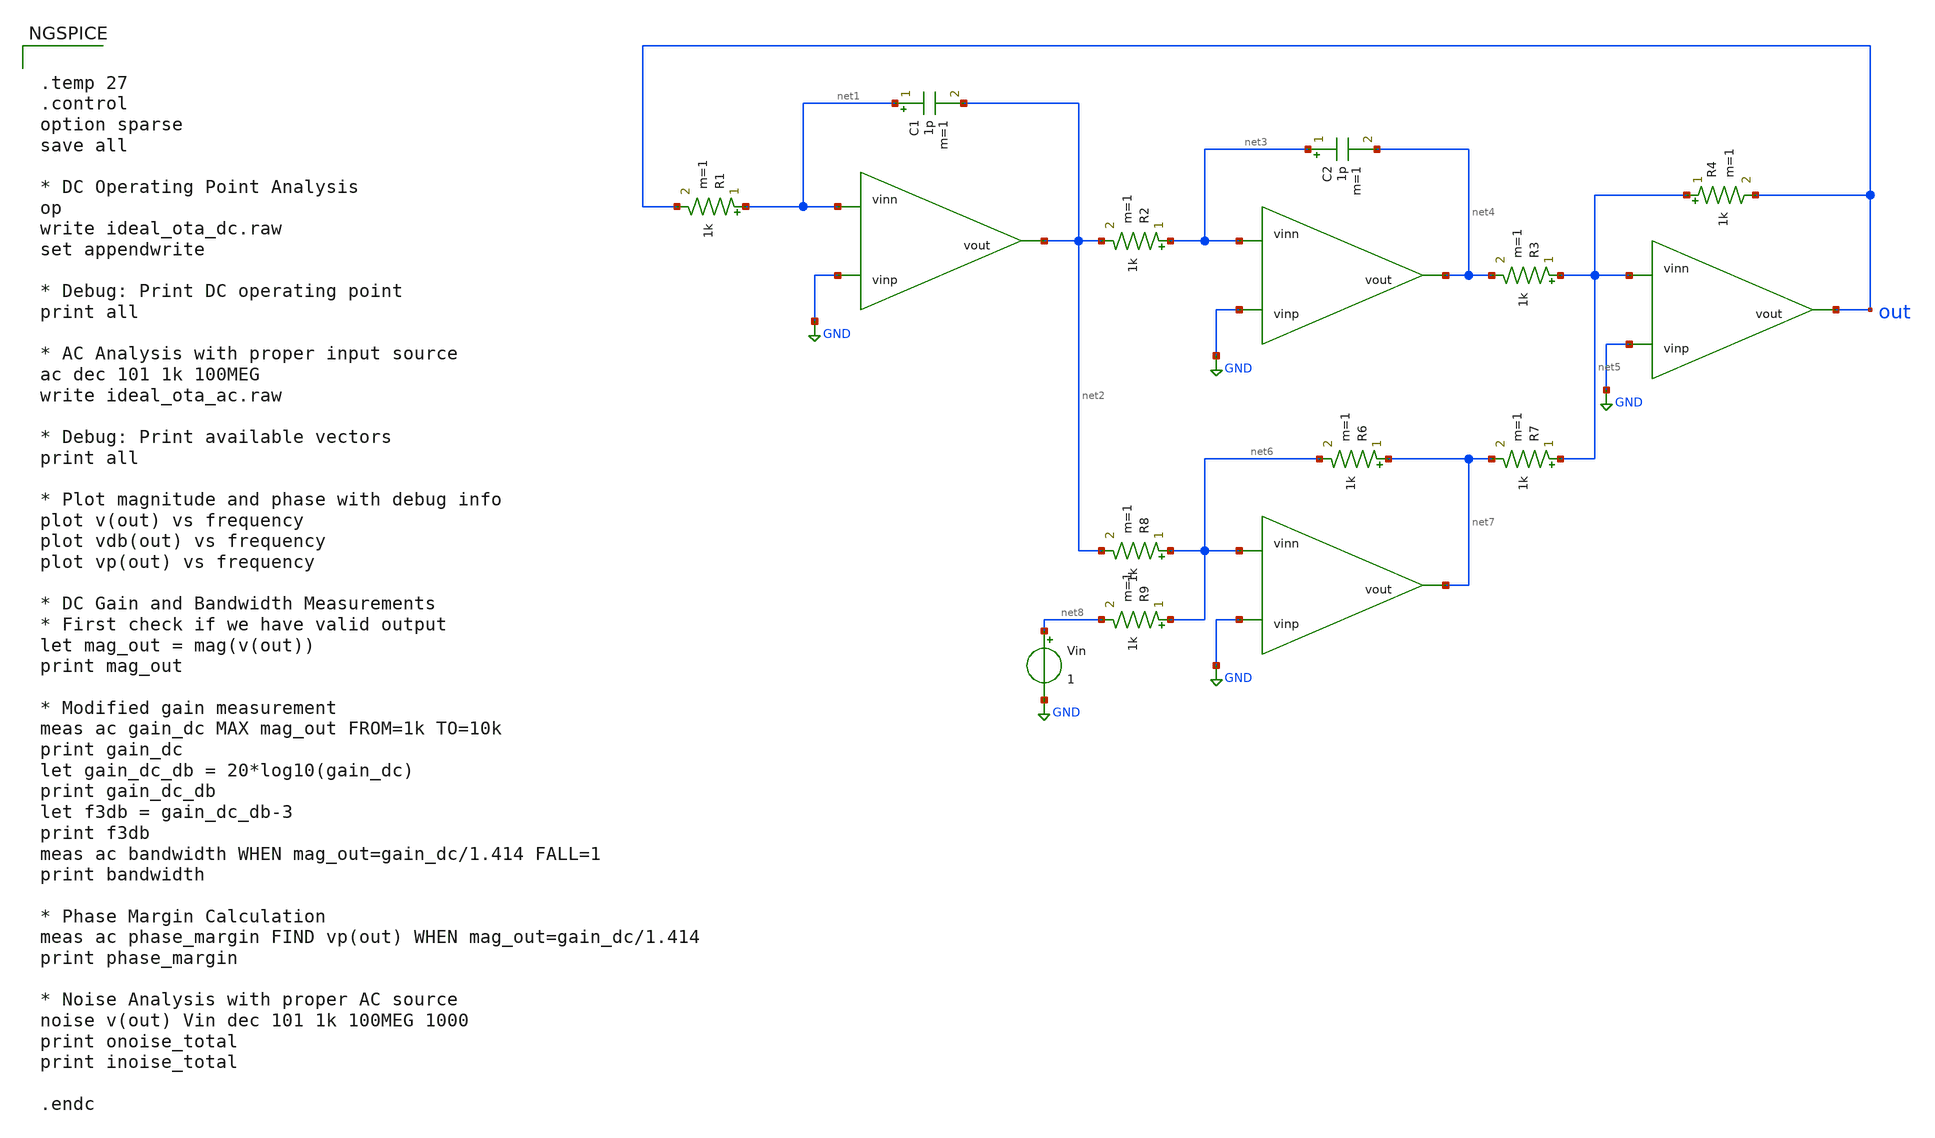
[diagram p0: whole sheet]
** sch_path: 2_Ideal_Cir/toplevel.sch
**.subckt toplevel
R1 net1 out 1k m=1
C1 net1 net2 1p m=1
R2 net3 net2 1k m=1
C2 net3 net4 1p m=1
R3 net5 net4 1k m=1
R4 net5 out 1k m=1
R6 net7 net6 1k m=1
R7 net5 net7 1k m=1
R8 net6 net2 1k m=1
R9 net6 net8 1k m=1
Vin net8 GND 1
**** begin user architecture code


.temp 27
.control
option sparse
save all

* DC Operating Point Analysis
op
write ideal_ota_dc.raw
set appendwrite

* Debug: Print DC operating point
print all

* AC Analysis with proper input source
ac dec 101 1k 100MEG
write ideal_ota_ac.raw

* Debug: Print available vectors
print all

* Plot magnitude and phase with debug info
plot v(out) vs frequency
plot vdb(out) vs frequency
plot vp(out) vs frequency

* DC Gain and Bandwidth Measurements
* First check if we have valid output
let mag_out = mag(v(out))
print mag_out

* Modified gain measurement
meas ac gain_dc MAX mag_out FROM=1k TO=10k
print gain_dc
let gain_dc_db = 20*log10(gain_dc)
print gain_dc_db
let f3db = gain_dc_db-3
print f3db
meas ac bandwidth WHEN mag_out=gain_dc/1.414 FALL=1
print bandwidth

* Phase Margin Calculation
meas ac phase_margin FIND vp(out) WHEN mag_out=gain_dc/1.414
print phase_margin

* Noise Analysis with proper AC source
noise v(out) Vin dec 101 1k 100MEG 1000
print onoise_total
print inoise_total

.endc


**** end user architecture code
**.ends
.GLOBAL GND
.end
